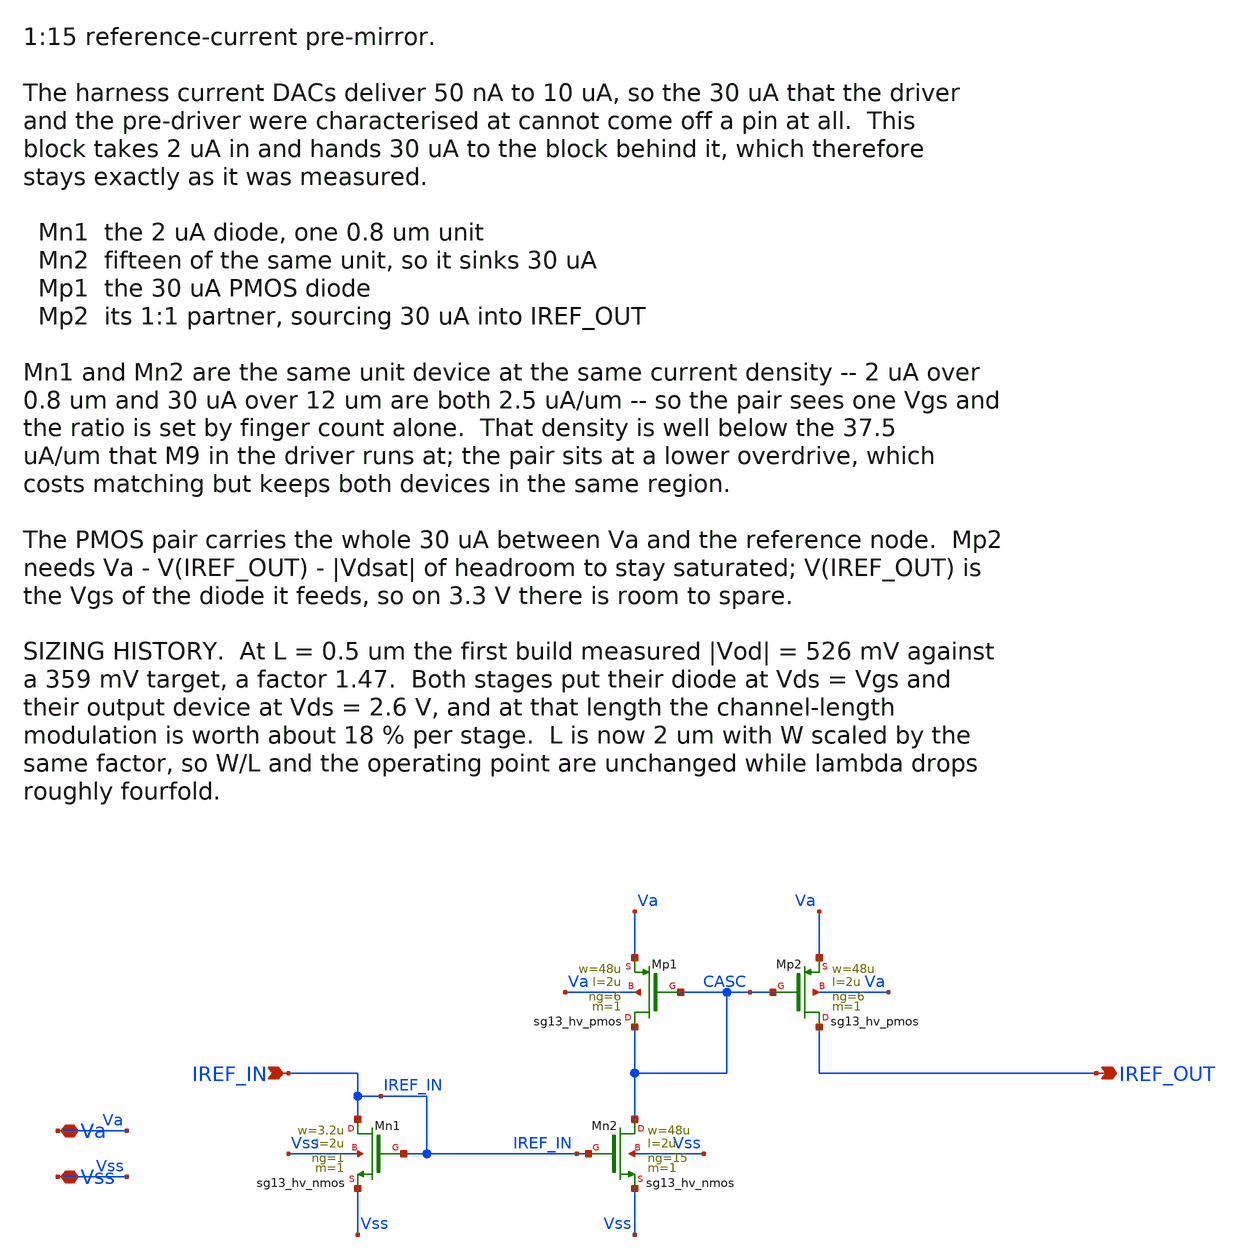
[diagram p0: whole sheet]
** sch_path: macros/lvds_tx/schematic/xschem/iref_x15.sch
**.subckt iref_x15 IREF_IN IREF_OUT Va Vss
*.ipin IREF_IN
*.opin IREF_OUT
*.iopin Va
*.iopin Vss
XMn1 IREF_IN IREF_IN Vss Vss sg13_hv_nmos w=3.2u l=2u ng=1 m=1 mm_ok=1
XMn2 CASC IREF_IN Vss Vss sg13_hv_nmos w=48u l=2u ng=15 m=1 mm_ok=1
XMp1 CASC CASC Va Va sg13_hv_pmos w=48u l=2u ng=6 m=1 mm_ok=1
XMp2 IREF_OUT CASC Va Va sg13_hv_pmos w=48u l=2u ng=6 m=1 mm_ok=1
**.ends
.end
